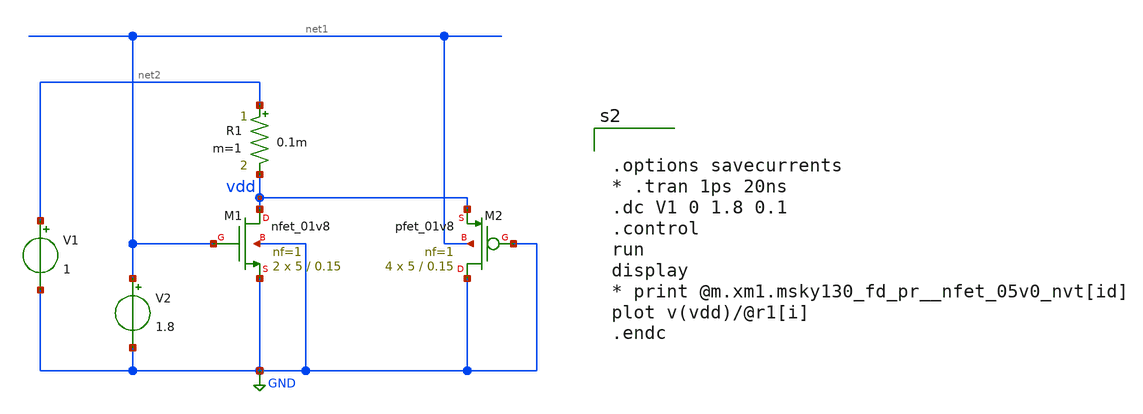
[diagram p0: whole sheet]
** sch_path: xschem/fet_impedance_tb.sch
**.subckt fet_impedance_tb
V1 net2 GND 1
V2 net1 GND 1.8
R1 net2 vdd 0.1m m=1
XM1 vdd net1 GND GND sky130_fd_pr__nfet_01v8 L=0.15 W=5 nf=1 ad='int((nf+1)/2) * W/nf * 0.29' as='int((nf+2)/2) * W/nf * 0.29'
+ pd='2*int((nf+1)/2) * (W/nf + 0.29)' ps='2*int((nf+2)/2) * (W/nf + 0.29)' nrd='0.29 / W' nrs='0.29 / W'
+ sa=0 sb=0 sd=0 mult=2 m=2
XM2 GND GND vdd net1 sky130_fd_pr__pfet_01v8 L=0.15 W=5 nf=1 ad='int((nf+1)/2) * W/nf * 0.29' as='int((nf+2)/2) * W/nf * 0.29'
+ pd='2*int((nf+1)/2) * (W/nf + 0.29)' ps='2*int((nf+2)/2) * (W/nf + 0.29)' nrd='0.29 / W' nrs='0.29 / W'
+ sa=0 sb=0 sd=0 mult=4 m=4
**** begin user architecture code
.lib $::SKYWATER_MODELS/sky130.lib.spice ff
* .include $::PDKPATH/libs.ref/sky130_fd_sc_hvl/spice/sky130_fd_sc_hvl.spice



.options savecurrents
* .tran 1ps 20ns
.dc V1 0 1.8 0.1
.control
run
display
* print @m.xm1.msky130_fd_pr__nfet_05v0_nvt[id]
plot v(vdd)/@r1[i]
.endc


**** end user architecture code
**.ends
.GLOBAL GND
.end
